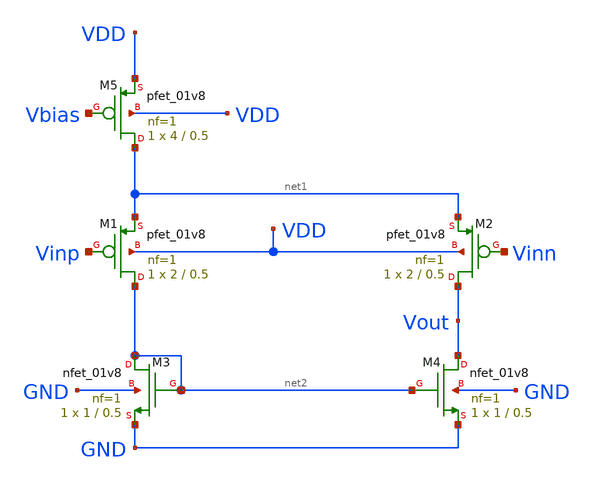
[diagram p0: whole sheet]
** sch_path: analog/build/schematic/opamp_single_stage.sch
**.subckt opamp_single_stage
XM5 net1 Vbias VDD VDD sky130_fd_pr__pfet_01v8 L=0.5 W=4 nf=1 ad='int((nf+1)/2) * W/nf * 0.29' as='int((nf+2)/2) * W/nf * 0.29'
+ pd='2*int((nf+1)/2) * (W/nf + 0.29)' ps='2*int((nf+2)/2) * (W/nf + 0.29)' nrd='0.29 / W' nrs='0.29 / W'
+ sa=0 sb=0 sd=0 mult=1 m=1
XM1 net2 Vinp net1 VDD sky130_fd_pr__pfet_01v8 L=0.5 W=2 nf=1 ad='int((nf+1)/2) * W/nf * 0.29' as='int((nf+2)/2) * W/nf * 0.29'
+ pd='2*int((nf+1)/2) * (W/nf + 0.29)' ps='2*int((nf+2)/2) * (W/nf + 0.29)' nrd='0.29 / W' nrs='0.29 / W'
+ sa=0 sb=0 sd=0 mult=1 m=1
XM2 Vout Vinn net1 VDD sky130_fd_pr__pfet_01v8 L=0.5 W=2 nf=1 ad='int((nf+1)/2) * W/nf * 0.29' as='int((nf+2)/2) * W/nf * 0.29'
+ pd='2*int((nf+1)/2) * (W/nf + 0.29)' ps='2*int((nf+2)/2) * (W/nf + 0.29)' nrd='0.29 / W' nrs='0.29 / W'
+ sa=0 sb=0 sd=0 mult=1 m=1
XM3 net2 net2 GND GND sky130_fd_pr__nfet_01v8 L=0.5 W=1 nf=1 ad='int((nf+1)/2) * W/nf * 0.29' as='int((nf+2)/2) * W/nf * 0.29'
+ pd='2*int((nf+1)/2) * (W/nf + 0.29)' ps='2*int((nf+2)/2) * (W/nf + 0.29)' nrd='0.29 / W' nrs='0.29 / W'
+ sa=0 sb=0 sd=0 mult=1 m=1
XM4 Vout net2 GND GND sky130_fd_pr__nfet_01v8 L=0.5 W=1 nf=1 ad='int((nf+1)/2) * W/nf * 0.29' as='int((nf+2)/2) * W/nf * 0.29'
+ pd='2*int((nf+1)/2) * (W/nf + 0.29)' ps='2*int((nf+2)/2) * (W/nf + 0.29)' nrd='0.29 / W' nrs='0.29 / W'
+ sa=0 sb=0 sd=0 mult=1 m=1
**.ends
.end
